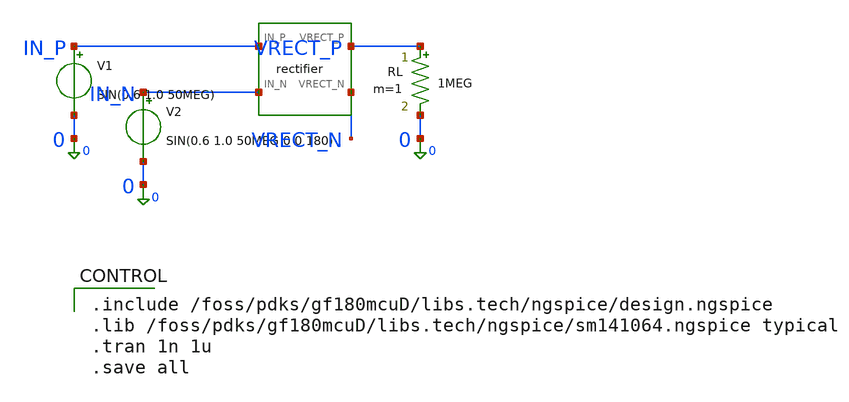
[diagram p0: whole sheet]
** sch_path: modules/PandaChip/designs/iris-harvester/exp/tb_rect_only.sch
**.subckt tb_rect_only
X4 IN_P IN_N VRECT_P VRECT_N rectifier
V1 IN_P 0 SIN(0.6 1.0 50MEG)
V2 IN_N 0 SIN(0.6 1.0 50MEG 0 0 180)
RL VRECT_P 0 1MEG m=1
**** begin user architecture code

.include /foss/pdks/gf180mcuD/libs.tech/ngspice/design.ngspice
.lib /foss/pdks/gf180mcuD/libs.tech/ngspice/sm141064.ngspice typical
.tran 1n 1u
.save all

**** end user architecture code
**.ends

* expanding   symbol:  rectifier.sym # of pins=4
** sym_path: modules/PandaChip/designs/iris-harvester/exp/rectifier.sym
** sch_path: modules/PandaChip/designs/iris-harvester/exp/rectifier.sch
.subckt rectifier IN_P IN_N VRECT_P VRECT_N
*.ipin IN_P
*.ipin IN_N
*.opin VRECT_P
*.opin VRECT_N
XM_P1 IN_P IN_N VRECT_P VRECT_P pfet_03v3 L=0.28u W=20u nf=2 ad='int((nf+1)/2) * W/nf * 0.18u' as='int((nf+2)/2) * W/nf * 0.18u'
+ pd='2*int((nf+1)/2) * (W/nf + 0.18u)' ps='2*int((nf+2)/2) * (W/nf + 0.18u)' nrd='0.18u / W' nrs='0.18u / W'
+ sa=0 sb=0 sd=0 m=1
XM_P2 IN_N IN_P VRECT_P VRECT_P pfet_03v3 L=0.28u W=20u nf=2 ad='int((nf+1)/2) * W/nf * 0.18u' as='int((nf+2)/2) * W/nf * 0.18u'
+ pd='2*int((nf+1)/2) * (W/nf + 0.18u)' ps='2*int((nf+2)/2) * (W/nf + 0.18u)' nrd='0.18u / W' nrs='0.18u / W'
+ sa=0 sb=0 sd=0 m=1
XM_N1 IN_P IN_N VRECT_N VRECT_N nfet_03v3 L=0.28u W=20u nf=2 ad='int((nf+1)/2) * W/nf * 0.18u' as='int((nf+2)/2) * W/nf * 0.18u'
+ pd='2*int((nf+1)/2) * (W/nf + 0.18u)' ps='2*int((nf+2)/2) * (W/nf + 0.18u)' nrd='0.18u / W' nrs='0.18u / W'
+ sa=0 sb=0 sd=0 m=1
XM_N2 IN_N IN_P VRECT_N VRECT_N nfet_03v3 L=0.28u W=20u nf=2 ad='int((nf+1)/2) * W/nf * 0.18u' as='int((nf+2)/2) * W/nf * 0.18u'
+ pd='2*int((nf+1)/2) * (W/nf + 0.18u)' ps='2*int((nf+2)/2) * (W/nf + 0.18u)' nrd='0.18u / W' nrs='0.18u / W'
+ sa=0 sb=0 sd=0 m=1
XM_D1 0 0 VRECT_N 0 nfet_03v3 L=0.28u W=10u nf=2 ad='int((nf+1)/2) * W/nf * 0.18u' as='int((nf+2)/2) * W/nf * 0.18u'
+ pd='2*int((nf+1)/2) * (W/nf + 0.18u)' ps='2*int((nf+2)/2) * (W/nf + 0.18u)' nrd='0.18u / W' nrs='0.18u / W'
+ sa=0 sb=0 sd=0 m=1
V_DUMMY1 VRECT_P DUMMY_NET1 0
V_DUMMY2 VRECT_N DUMMY_NET2 0
.ends

.end
